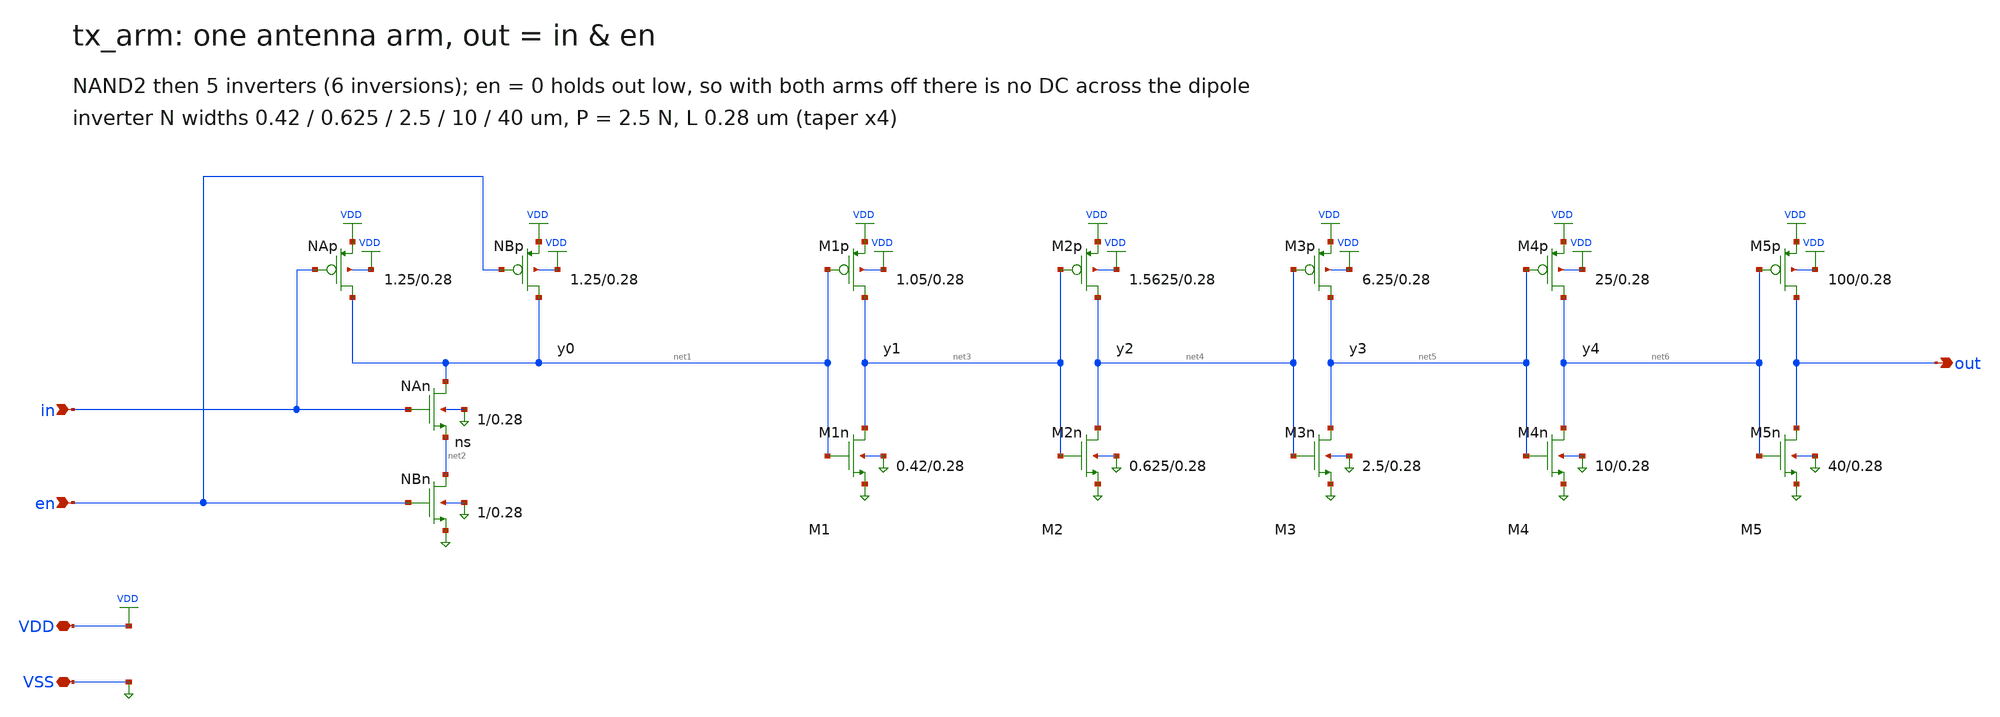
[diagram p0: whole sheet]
** sch_path: xschem/tx_arm.sch
**.subckt tx_arm VDD VSS in en out
*.iopin VDD
*.iopin VSS
*.ipin in
*.ipin en
*.opin out
XNAp net1 in VDD VDD pfet_03v3 L=0.28u W=1.25u nf=1 ad=0.625p as=0.625p pd=3.5u ps=3.5u nrd=0 nrs=0
+ sa=0 sb=0 sd=0 m=1
XNBp net1 en VDD VDD pfet_03v3 L=0.28u W=1.25u nf=1 ad=0.625p as=0.625p pd=3.5u ps=3.5u nrd=0 nrs=0
+ sa=0 sb=0 sd=0 m=1
XNAn net1 in net2 VSS nfet_03v3 L=0.28u W=1.0u nf=1 ad=0.5p as=0.5p pd=3.0u ps=3.0u nrd=0 nrs=0 sa=0
+ sb=0 sd=0 m=1
XNBn net2 en VSS VSS nfet_03v3 L=0.28u W=1.0u nf=1 ad=0.5p as=0.5p pd=3.0u ps=3.0u nrd=0 nrs=0 sa=0
+ sb=0 sd=0 m=1
XM1p net3 net1 VDD VDD pfet_03v3 L=0.28u W=1.0499999999999998u nf=1 ad=0.5249999999999999p
+ as=0.5249999999999999p pd=3.0999999999999996u ps=3.0999999999999996u nrd=0 nrs=0 sa=0 sb=0 sd=0 m=1
XM1n net3 net1 VSS VSS nfet_03v3 L=0.28u W=0.41999999999999993u nf=1 ad=0.20999999999999996p
+ as=0.20999999999999996p pd=1.8399999999999999u ps=1.8399999999999999u nrd=0 nrs=0 sa=0 sb=0 sd=0 m=1
XM2p net4 net3 VDD VDD pfet_03v3 L=0.28u W=1.5624999999999998u nf=1 ad=0.7812499999999999p
+ as=0.7812499999999999p pd=4.125u ps=4.125u nrd=0 nrs=0 sa=0 sb=0 sd=0 m=1
XM2n net4 net3 VSS VSS nfet_03v3 L=0.28u W=0.625u nf=1 ad=0.3125p as=0.3125p pd=2.25u ps=2.25u nrd=0
+ nrs=0 sa=0 sb=0 sd=0 m=1
XM3p net5 net4 VDD VDD pfet_03v3 L=0.28u W=6.249999999999999u nf=1 ad=3.1249999999999996p
+ as=3.1249999999999996p pd=13.499999999999998u ps=13.499999999999998u nrd=0 nrs=0 sa=0 sb=0 sd=0 m=1
XM3n net5 net4 VSS VSS nfet_03v3 L=0.28u W=2.5u nf=1 ad=1.25p as=1.25p pd=6.0u ps=6.0u nrd=0 nrs=0
+ sa=0 sb=0 sd=0 m=1
XM4p net6 net5 VDD VDD pfet_03v3 L=0.28u W=24.999999999999996u nf=1 ad=12.499999999999998p
+ as=12.499999999999998p pd=50.99999999999999u ps=50.99999999999999u nrd=0 nrs=0 sa=0 sb=0 sd=0 m=1
XM4n net6 net5 VSS VSS nfet_03v3 L=0.28u W=10.0u nf=1 ad=5.0p as=5.0p pd=21.0u ps=21.0u nrd=0 nrs=0
+ sa=0 sb=0 sd=0 m=1
XM5p out net6 VDD VDD pfet_03v3 L=0.28u W=99.99999999999999u nf=1 ad=49.99999999999999p
+ as=49.99999999999999p pd=200.99999999999997u ps=200.99999999999997u nrd=0 nrs=0 sa=0 sb=0 sd=0 m=1
XM5n out net6 VSS VSS nfet_03v3 L=0.28u W=40.0u nf=1 ad=20.0p as=20.0p pd=81.0u ps=81.0u nrd=0 nrs=0
+ sa=0 sb=0 sd=0 m=1
**.ends
.end
